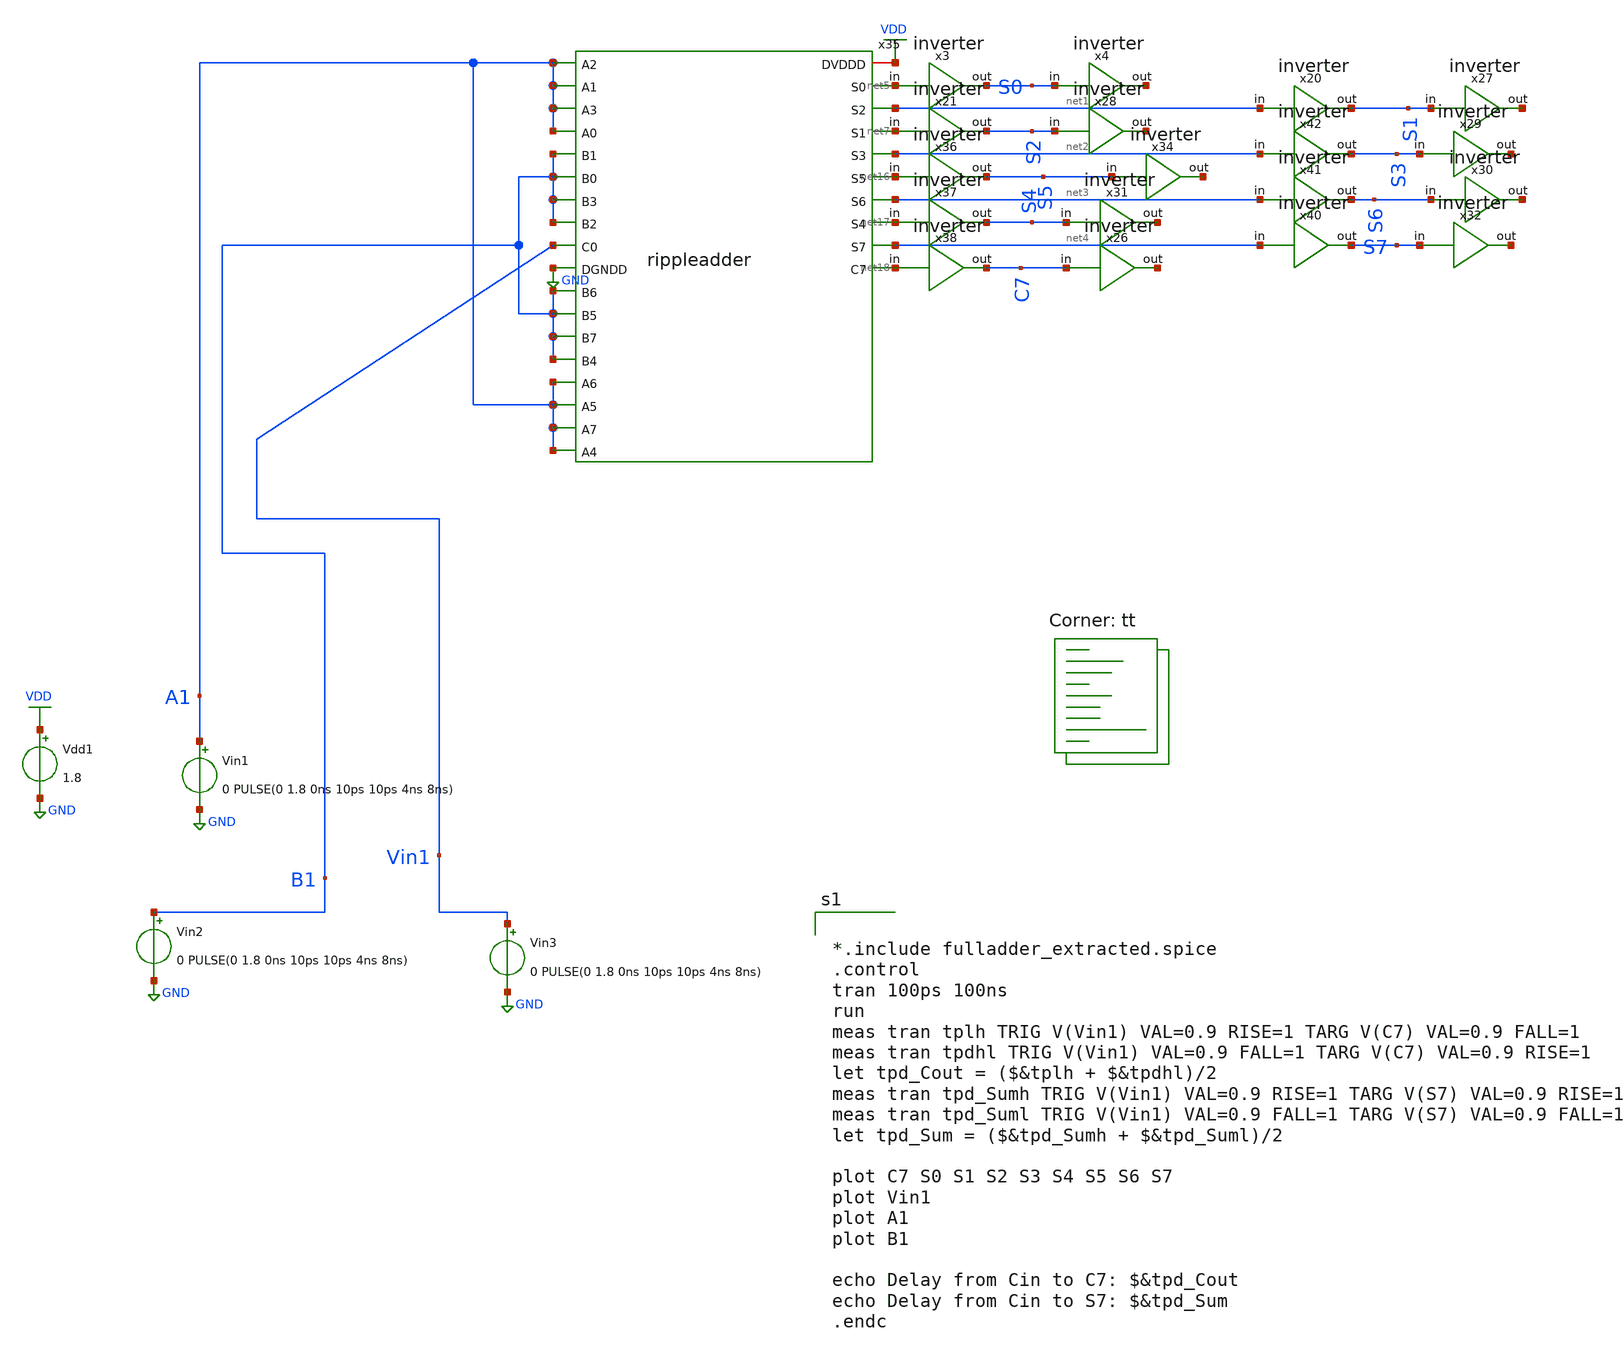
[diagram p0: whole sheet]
** sch_path: Tutorial_6/Part-B/final.sch
**.subckt final
x3 S0 net5 inverter
Vdd1 VDD GND 1.8
x4 net6 S0 inverter
Vin2 B1 GND 0 PULSE(0 1.8 0ns 10ps 10ps 4ns 8ns)
Vin1 A1 GND 0 PULSE(0 1.8 0ns 10ps 10ps 4ns 8ns)
Vin3 Vin1 GND 0 PULSE(0 1.8 0ns 10ps 10ps 4ns 8ns)
x20 S1 net1 inverter
x21 S2 net7 inverter
x26 net8 C7 inverter
x27 net9 S1 inverter
x28 net10 S2 inverter
x29 net11 S3 inverter
x30 net12 S6 inverter
x31 net13 S4 inverter
x32 net14 S7 inverter
x34 net15 S5 inverter
x35 VDD A1 A1 A1 A1 B1 B1 B1 B1 net5 net1 net7 Vin1 net2 GND net16 net3 net17 net4 B1 B1 net18 B1 B1
+ A1 A1 A1 A1 rippleadder
x36 S5 net16 inverter
x37 S4 net17 inverter
x38 C7 net18 inverter
x40 S7 net4 inverter
x41 S6 net3 inverter
x42 S3 net2 inverter
**** begin user architecture code


*.include fulladder_extracted.spice
.control
tran 100ps 100ns
run
meas tran tplh TRIG V(Vin1) VAL=0.9 RISE=1 TARG V(C7) VAL=0.9 FALL=1
meas tran tpdhl TRIG V(Vin1) VAL=0.9 FALL=1 TARG V(C7) VAL=0.9 RISE=1
let tpd_Cout = ($&tplh + $&tpdhl)/2
meas tran tpd_Sumh TRIG V(Vin1) VAL=0.9 RISE=1 TARG V(S7) VAL=0.9 RISE=1
meas tran tpd_Suml TRIG V(Vin1) VAL=0.9 FALL=1 TARG V(S7) VAL=0.9 FALL=1
let tpd_Sum = ($&tpd_Sumh + $&tpd_Suml)/2

plot C7 S0 S1 S2 S3 S4 S5 S6 S7
plot Vin1
plot A1
plot B1

echo Delay from Cin to C7: $&tpd_Cout
echo Delay from Cin to S7: $&tpd_Sum
.endc



.lib $::SKYWATER_MODELS/sky130.lib.spice tt
**** end user architecture code
**.ends
.GLOBAL GND
.GLOBAL VDD
.end
